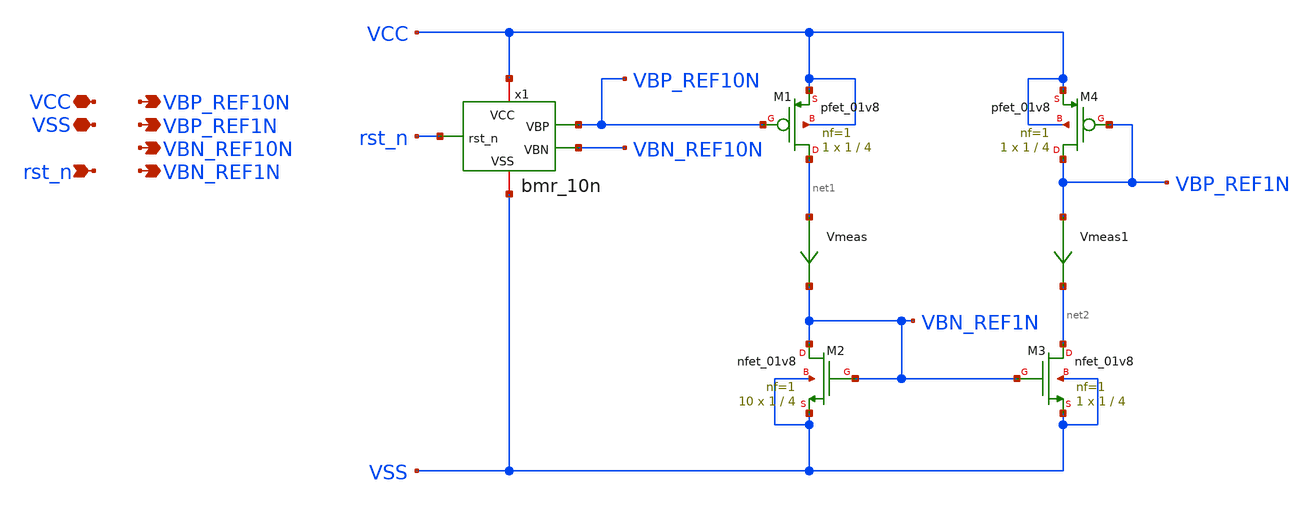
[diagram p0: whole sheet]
** sch_path: schem/bias/bmr.sch
**.subckt bmr VCC VSS rst_n VBP_REF10N VBP_REF1N VBN_REF10N VBN_REF1N
*.iopin VCC
*.iopin VSS
*.ipin rst_n
*.opin VBP_REF10N
*.opin VBP_REF1N
*.opin VBN_REF10N
*.opin VBN_REF1N
x1 VCC VBP_REF10N VSS VBN_REF10N rst_n bmr_10n
XM1 net1 VBP_REF10N VCC VCC sky130_fd_pr__pfet_01v8 L=4 W=1 nf=1 ad='int((1 + 1)/2) * 1 / 1 * 0.29' as='int((1 + 2)/2) * 1 / 1 * 0.29'
+ pd='2*int((1 + 1)/2) * (1 / 1 + 0.29)' ps='2*int((1 + 2)/2) * (1 / 1 + 0.29)' nrd='0.29 / 1 ' nrs='0.29 / 1 '
+ sa=0 sb=0 sd=0 mult=1 m=1
XM2 VBN_REF1N VBN_REF1N VSS VSS sky130_fd_pr__nfet_01v8 L=4 W=1 nf=1 ad='int((1 + 1)/2) * 1 / 1 * 0.29'
+ as='int((1 + 2)/2) * 1 / 1 * 0.29' pd='2*int((1 + 1)/2) * (1 / 1 + 0.29)' ps='2*int((1 + 2)/2) * (1 / 1 + 0.29)'
+ nrd='0.29 / 1 ' nrs='0.29 / 1 ' sa=0 sb=0 sd=0 mult=10 m=10
XM3 net2 VBN_REF1N VSS VSS sky130_fd_pr__nfet_01v8 L=4 W=1 nf=1 ad='int((1 + 1)/2) * 1 / 1 * 0.29' as='int((1 + 2)/2) * 1 / 1 * 0.29'
+ pd='2*int((1 + 1)/2) * (1 / 1 + 0.29)' ps='2*int((1 + 2)/2) * (1 / 1 + 0.29)' nrd='0.29 / 1 ' nrs='0.29 / 1 '
+ sa=0 sb=0 sd=0 mult=1 m=1
XM4 VBP_REF1N VBP_REF1N VCC VCC sky130_fd_pr__pfet_01v8 L=4 W=1 nf=1 ad='int((1 + 1)/2) * 1 / 1 * 0.29'
+ as='int((1 + 2)/2) * 1 / 1 * 0.29' pd='2*int((1 + 1)/2) * (1 / 1 + 0.29)' ps='2*int((1 + 2)/2) * (1 / 1 + 0.29)'
+ nrd='0.29 / 1 ' nrs='0.29 / 1 ' sa=0 sb=0 sd=0 mult=1 m=1
Vmeas net1 VBN_REF1N 0
.save i(vmeas)
Vmeas1 VBP_REF1N net2 0
.save i(vmeas1)
**.ends

* expanding   symbol:  bias/bmr_10n.sym # of pins=5
** sym_path: schem/bias/bmr_10n.sym
** sch_path: schem/bias/bmr_10n.sch
.subckt bmr_10n VCC VBP VSS VBN rst_n
*.iopin VCC
*.iopin VSS
*.ipin rst_n
*.opin VBP
*.opin VBN
XM1 VBP VBP VCC VCC sky130_fd_pr__pfet_01v8 L=4 W=1 nf=1 ad='int((1 + 1)/2) * 1 / 1 * 0.29' as='int((1 + 2)/2) * 1 / 1 * 0.29'
+ pd='2*int((1 + 1)/2) * (1 / 1 + 0.29)' ps='2*int((1 + 2)/2) * (1 / 1 + 0.29)' nrd='0.29 / 1 ' nrs='0.29 / 1 '
+ sa=0 sb=0 sd=0 mult=1 m=1
XM2 net3 VBP VCC VCC sky130_fd_pr__pfet_01v8 L=4 W=1 nf=1 ad='int((1 + 1)/2) * 1 / 1 * 0.29' as='int((1 + 2)/2) * 1 / 1 * 0.29'
+ pd='2*int((1 + 1)/2) * (1 / 1 + 0.29)' ps='2*int((1 + 2)/2) * (1 / 1 + 0.29)' nrd='0.29 / 1 ' nrs='0.29 / 1 '
+ sa=0 sb=0 sd=0 mult=1 m=1
XM3 net2 VBN net1 VSS sky130_fd_pr__nfet_01v8 L=4 W=8 nf=1 ad='int((1 + 1)/2) * 8 / 1 * 0.29' as='int((1 + 2)/2) * 8 / 1 * 0.29'
+ pd='2*int((1 + 1)/2) * (8 / 1 + 0.29)' ps='2*int((1 + 2)/2) * (8 / 1 + 0.29)' nrd='0.29 / 8 ' nrs='0.29 / 8 '
+ sa=0 sb=0 sd=0 mult=1 m=1
XM4 VBN VBN VSS VSS sky130_fd_pr__nfet_01v8 L=4 W=1 nf=1 ad='int((1 + 1)/2) * 1 / 1 * 0.29' as='int((1 + 2)/2) * 1 / 1 * 0.29'
+ pd='2*int((1 + 1)/2) * (1 / 1 + 0.29)' ps='2*int((1 + 2)/2) * (1 / 1 + 0.29)' nrd='0.29 / 1 ' nrs='0.29 / 1 '
+ sa=0 sb=0 sd=0 mult=1 m=1
XR1 net5 net1 net4 sky130_fd_pr__res_xhigh_po_0p35 L={LR} mult=1 m=1
VSRIGHT VBP net2 0
.save i(vsright)
VSLEFT net3 VBN 0
.save i(vsleft)
XM5 VBN rst_n VCC VCC sky130_fd_pr__pfet_01v8 L=4 W=1 nf=1 ad='int((1 + 1)/2) * 1 / 1 * 0.29' as='int((1 + 2)/2) * 1 / 1 * 0.29'
+ pd='2*int((1 + 1)/2) * (1 / 1 + 0.29)' ps='2*int((1 + 2)/2) * (1 / 1 + 0.29)' nrd='0.29 / 1 ' nrs='0.29 / 1 '
+ sa=0 sb=0 sd=0 mult=1 m=1
XR2 net6 net5 net4 sky130_fd_pr__res_xhigh_po_0p35 L={LR} mult=1 m=1
XR3 net7 net6 net4 sky130_fd_pr__res_xhigh_po_0p35 L={LR} mult=1 m=1
XR4 net8 net7 net4 sky130_fd_pr__res_xhigh_po_0p35 L={LR} mult=1 m=1
XR5 net9 net8 net4 sky130_fd_pr__res_xhigh_po_0p35 L={LR} mult=1 m=1
XR6 net10 net9 net4 sky130_fd_pr__res_xhigh_po_0p35 L={LR} mult=1 m=1
XR7 net11 net10 net4 sky130_fd_pr__res_xhigh_po_0p35 L={LR} mult=1 m=1
XR8 VSS net11 net4 sky130_fd_pr__res_xhigh_po_0p35 L={LR} mult=1 m=1
**** begin user architecture code


.param LR=1084/8


**** end user architecture code
.ends

.end
